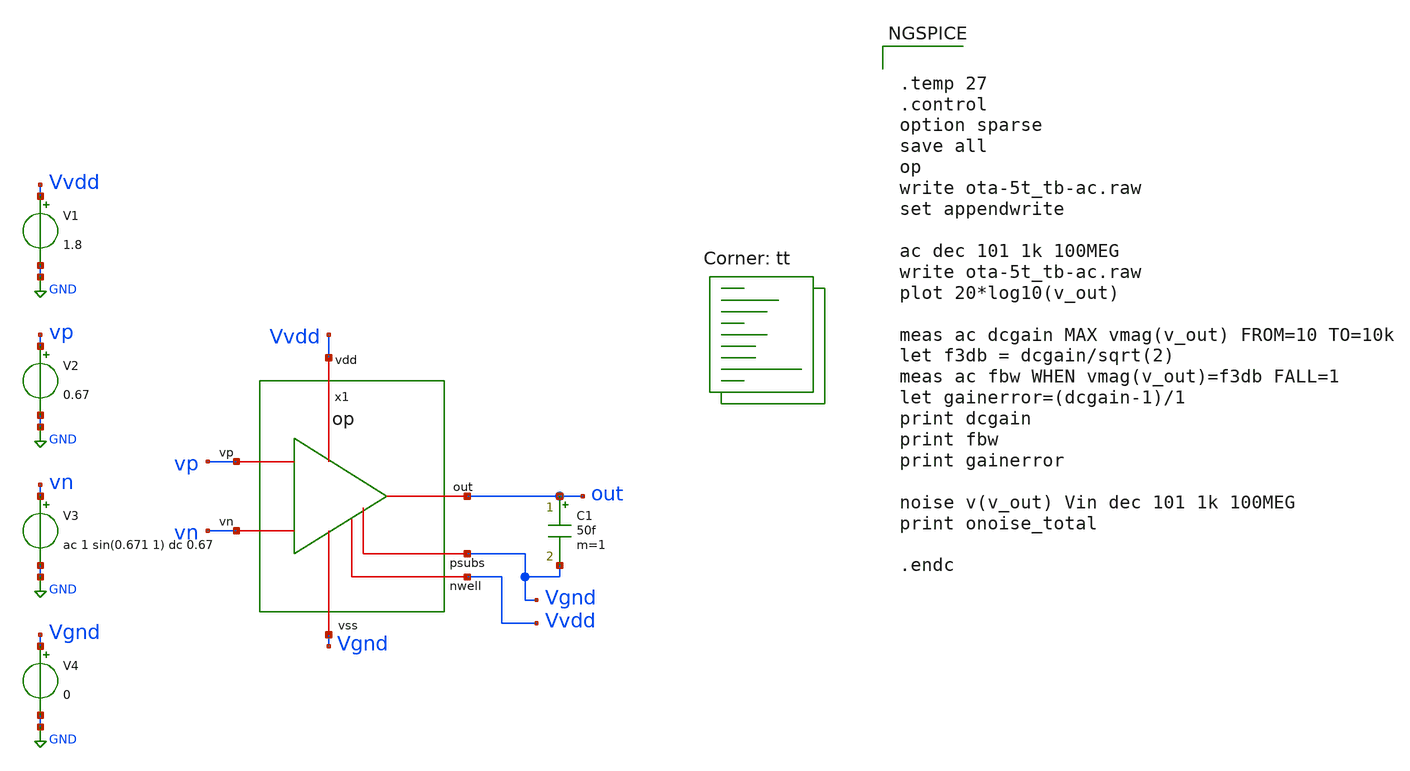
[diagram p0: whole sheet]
** sch_path: xschem/op_tb.sch
**.subckt op_tb
V1 Vvdd GND 1.8
V2 vp GND 0.67
V3 vn GND ac 1 sin(0.671 1) dc 0.67
x1 out Vvdd Vgnd vp vn Vgnd Vvdd op
V4 Vgnd GND 0
C1 out Vgnd 50f m=1
**** begin user architecture code
.lib $::SKYWATER_MODELS/sky130.lib.spice tt


.temp 27
.control
option sparse
save all
op
write ota-5t_tb-ac.raw
set appendwrite

ac dec 101 1k 100MEG
write ota-5t_tb-ac.raw
plot 20*log10(v_out)

meas ac dcgain MAX vmag(v_out) FROM=10 TO=10k
let f3db = dcgain/sqrt(2)
meas ac fbw WHEN vmag(v_out)=f3db FALL=1
let gainerror=(dcgain-1)/1
print dcgain
print fbw
print gainerror

noise v(v_out) Vin dec 101 1k 100MEG
print onoise_total

.endc


**** end user architecture code
**.ends

* expanding   symbol:  op.sym # of pins=7
** sym_path: xschem/op.sym
** sch_path: xschem/op.sch
.subckt op out vdd vss vp vn psubs nwell
*.iopin vss
*.iopin vdd
*.opin out
*.ipin vp
*.ipin vn
*.iopin psubs
*.iopin nwell
XM3 out net1 vdd nwell sky130_fd_pr__pfet_01v8 L={l3} W={w3} nf={nf3} ad='int((nf+1)/2) * W/nf * 0.29'
+ as='int((nf+2)/2) * W/nf * 0.29' pd='2*int((nf+1)/2) * (W/nf + 0.29)' ps='2*int((nf+2)/2) * (W/nf + 0.29)'
+ nrd='0.29 / W' nrs='0.29 / W' sa=0 sb=0 sd=0 mult=1 m=1
XM1b net1 vn net2 psubs sky130_fd_pr__nfet_01v8 L={l1} W={w1} nf={nf1} ad='int((nf+1)/2) * W/nf * 0.29'
+ as='int((nf+2)/2) * W/nf * 0.29' pd='2*int((nf+1)/2) * (W/nf + 0.29)' ps='2*int((nf+2)/2) * (W/nf + 0.29)'
+ nrd='0.29 / W' nrs='0.29 / W' sa=0 sb=0 sd=0 mult=1 m=1
XM1a net3 vp net2 psubs sky130_fd_pr__nfet_01v8 L={l1} W={w1} nf={nf1} ad='int((nf+1)/2) * W/nf * 0.29'
+ as='int((nf+2)/2) * W/nf * 0.29' pd='2*int((nf+1)/2) * (W/nf + 0.29)' ps='2*int((nf+2)/2) * (W/nf + 0.29)'
+ nrd='0.29 / W' nrs='0.29 / W' sa=0 sb=0 sd=0 mult=1 m=1
XR1 net4 net1 vss sky130_fd_pr__res_high_po_0p35 L={lrz} mult=1 m=1
XC1 out net4 sky130_fd_pr__cap_mim_m3_1 W={wc} L={wc} MF={mc} m={mc}
**** begin user architecture code


.include ../sizing_opamp.spice


**** end user architecture code
XM2a net3 net3 vdd nwell sky130_fd_pr__pfet_01v8 L={l2} W={w2} nf={nf2} ad='int(({nf2} + 1)/2) * {w2} / {nf2} * 0.29'
+ as='int(({nf2} + 2)/2) * {w2} / {nf2} * 0.29' pd='2*int(({nf2} + 1)/2) * ({w2} / {nf2} + 0.29)' ps='2*int(({nf2} + 2)/2) * ({w2} / {nf2} + 0.29)'
+ nrd='0.29 / {w2} ' nrs='0.29 / {w2} ' sa=0 sb=0 sd=0 mult=1 m=1
XM2b net1 net3 vdd nwell sky130_fd_pr__pfet_01v8 L={l2} W={w2} nf={nf2} ad='int(({nf2} + 1)/2) * {w2} / {nf2} * 0.29'
+ as='int(({nf2} + 2)/2) * {w2} / {nf2} * 0.29' pd='2*int(({nf2} + 1)/2) * ({w2} / {nf2} + 0.29)' ps='2*int(({nf2} + 2)/2) * ({w2} / {nf2} + 0.29)'
+ nrd='0.29 / {w2} ' nrs='0.29 / {w2} ' sa=0 sb=0 sd=0 mult=1 m=1
XM0a bias bias vss psubs sky130_fd_pr__nfet_01v8 L={l0} W={w0} nf={nf0} ad='int(({nf0} + 1)/2) * {w0} / {nf0} * 0.29'
+ as='int(({nf0} + 2)/2) * {w0} / {nf0} * 0.29' pd='2*int(({nf0} + 1)/2) * ({w0} / {nf0} + 0.29)' ps='2*int(({nf0} + 2)/2) * ({w0} / {nf0} + 0.29)'
+ nrd='0.29 / {w0} ' nrs='0.29 / {w0} ' sa=0 sb=0 sd=0 mult=1 m=1
I0 vdd bias {i_tail}
XM0b net2 bias vss psubs sky130_fd_pr__nfet_01v8 L={l0} W={w0} nf={nf0} ad='int(({nf0} + 1)/2) * {w0} / {nf0} * 0.29'
+ as='int(({nf0} + 2)/2) * {w0} / {nf0} * 0.29' pd='2*int(({nf0} + 1)/2) * ({w0} / {nf0} + 0.29)' ps='2*int(({nf0} + 2)/2) * ({w0} / {nf0} + 0.29)'
+ nrd='0.29 / {w0} ' nrs='0.29 / {w0} ' sa=0 sb=0 sd=0 mult=1 m=1
XM0c out bias vss psubs sky130_fd_pr__nfet_01v8 L={l0} W={w0} nf={nf0} ad='int(({nf0} + 1)/2) * {w0} / {nf0} * 0.29'
+ as='int(({nf0} + 2)/2) * {w0} / {nf0} * 0.29' pd='2*int(({nf0} + 1)/2) * ({w0} / {nf0} + 0.29)' ps='2*int(({nf0} + 2)/2) * ({w0} / {nf0} + 0.29)'
+ nrd='0.29 / {w0} ' nrs='0.29 / {w0} ' sa=0 sb=0 sd=0 mult=1 m=1
.ends

.GLOBAL GND
.end
